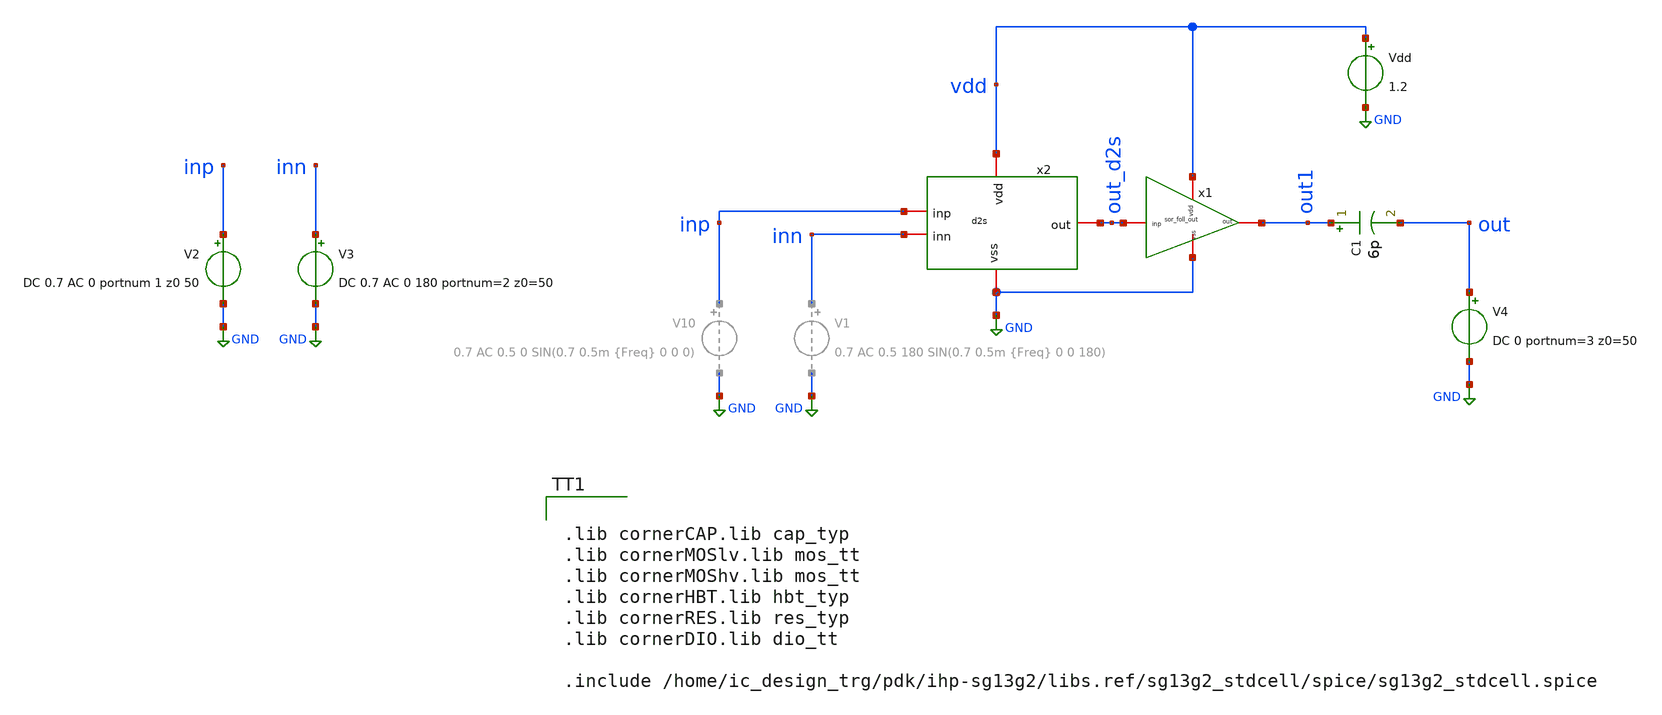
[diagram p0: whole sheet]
** sch_path: LNA7096-main/schematic/xschem/05a_d2s/d2s_tran.sch
* Copyright 2023 IHP PDK Authors
**.subckt d2s_tran
Vdd vdd GND 1.2
x2 vdd out_d2s inp inn GND d2s
V2 inp GND DC 0.7 AC 0 portnum 1 z0 50
V3 inn GND DC 0.7 AC 0 180 portnum=2 z0=50
V4 out GND DC 0 portnum=3 z0=50
x1 vdd out_d2s out1 GND sor_foll_out
C1 out1 out 6p m=1
**** begin user architecture code

.lib cornerCAP.lib cap_typ
.lib cornerMOSlv.lib mos_tt
.lib cornerMOShv.lib mos_tt
.lib cornerHBT.lib hbt_typ
.lib cornerRES.lib res_typ
.lib cornerDIO.lib dio_tt

.include /home/ic_design_trg/pdk/ihp-sg13g2/libs.ref/sg13g2_stdcell/spice/sg13g2_stdcell.spice



.include /home/ic_design_trg/lna_ihp/xschem/05a_d2s/simulation/d2s_tran.save
.param temp=27
.param Freq=1.176e9

.control
** 1. Initial Setup and OP Analysis
* FORCE ngspice to keep all nodes and S-parameters in memory
* (Crucial since the external .save file will otherwise discard them)
save all S_1_1 S_2_2 S_3_3 S_3_1 S_3_2
unset appendwrite

op
remzerovec
write d2s_tran.raw all
set appendwrite

** 2. S-Parameter Analysis
sp dec 100 100meg 5g

    * A. Calculate standard RF metrics in dB
    let s11_db = db(S_1_1)  $ Input Reflection (Port 1)
    let s22_db = db(S_2_2)  $ Input Reflection (Port 2)
    let s33_db = db(S_3_3)  $ Output Reflection (Port 3)
    let s31_db = db(S_3_1)  $ Forward Power Gain (Port 1 to 3)
    let s32_db = db(S_3_2)  $ Forward Power Gain (Port 2 to 3)

    * =============================================================
    * B. MIXED-MODE S-PARAMETERS
    * Calculate Differential-to-Single-Ended transfer function (S_sd)
    * =============================================================
    let S_sd = (S_3_1 - S_3_2) / sqrt(2)

    * Calculate the Gain (dB) and Phase (Degrees) of the differential signal
    let gain_diff_db = db(S_sd)
    let phase_diff_deg = cph(S_sd) * 180 / pi

    * C. Measure Matching at L5 Center (1.176 GHz)
    meas sp s11_l5 find s11_db at=1.176g
    meas sp s33_l5 find s33_db at=1.176g

    * D. Measure Single-Ended and Differential Gain/Phase at 1.176 GHz
    meas sp s31_l5 find s31_db at=1.176g
    meas sp gain_diff_l5 find gain_diff_db at=1.176g
    meas sp phase_diff_l5 find phase_diff_deg at=1.176g

** 3. Save and Plot SP Results
    * Explicitly include the newly calculated dB vectors, complex S-params, and mixed-mode vectors
    write d2s_tran.raw S_1_1 S_3_3 S_3_1 S_3_2 S_sd s11_db s33_db s31_db s22_db s32_db gain_diff_db
+ phase_diff_deg

    * Plot standard Single-Ended S-Parameters
    set xbrushwidth=2
    plot s11_db s33_db title 'Return Loss (dB)' ylabel 'Magnitude (dB)'
    plot s31_db s32_db title 'Single-Ended S-Parameters (dB)' ylabel 'Magnitude (dB)'

    * Plot the Calculated Differential-to-Single-Ended results
    plot gain_diff_db title 'Diff-to-Single-Ended Gain (dB)' ylabel 'Magnitude (dB)'
    plot phase_diff_deg title 'Diff-to-Single-Ended Phase (Deg)' ylabel 'Phase (Deg)'

.endc


**** end user architecture code
**.ends

* expanding   symbol:  05a_d2s/d2s.sym # of pins=5
** sym_path: LNA7096-main/schematic/xschem/05a_d2s/d2s.sym
** sch_path: LNA7096-main/schematic/xschem/05a_d2s/d2s.sch
.subckt d2s vdd out inp inn vss
*.iopin vdd
*.iopin vss
*.iopin out
*.iopin inp
*.iopin inn
XR3 vdd out1 vss rppd w=2e-6 l=1.52e-6 m=1 b=0 mm_ok=1
XR1 vdd out vss rppd w=2e-6 l=1.52e-6 m=1 b=0 mm_ok=1
XM2 out1 inp n1 net1 sg13_lv_nmos w=100u l=0.15u ng=20 m=1 mm_ok=1
XD5 net1 vdd vss isolbox l=15u w=10u
XR22 n1 net1 ptap1 R=64.81 w=0.39e-6 l=6e-6
XM5 n1 bias vss vss sg13_lv_nmos w=130u l=0.15u ng=40 m=1 mm_ok=1
XM1 out inn n1 net2 sg13_lv_nmos w=100u l=0.15u ng=20 m=1 mm_ok=1
XD1 net2 vdd vss isolbox l=15u w=10u
XR2 n1 net2 ptap1 R=64.81 w=0.39e-6 l=6e-6
XM3 bias bias vss vss sg13_lv_nmos w=5u l=0.15u ng=2 m=1 mm_ok=1
XR4 vdd bias vss rppd w=1e-6 l=24e-6 m=1 b=0 mm_ok=1
.ends


* expanding   symbol:  03_sor_foll/sor_foll_out.sym # of pins=4
** sym_path: LNA7096-main/schematic/xschem/03_sor_foll/sor_foll_out.sym
** sch_path: LNA7096-main/schematic/xschem/03_sor_foll/sor_foll_out.sch
.subckt sor_foll_out vdd inp out vss
*.iopin vdd
*.iopin vss
*.iopin inp
*.iopin out
XR3 vdd n8 vss rhigh w=1e-6 l=5e-6 m=1 b=0 mm_ok=1
XM3 out n8 vss vss sg13_lv_nmos w=85.925u l=0.25u ng=35 m=1 mm_ok=1
XM2 n8 n8 vss vss sg13_lv_nmos w=5u l=0.25u ng=1 m=1 mm_ok=1
XM1 vdd inp out net1 sg13_lv_nmos w=184.86u l=0.25u ng=20 m=1 mm_ok=1
XD1 net1 vdd vss isolbox l=29.14u w=10.735u
XR1 out net1 ptap1 R=55.97 w=0.39e-6 l=7e-6
.ends

.GLOBAL GND
.end
